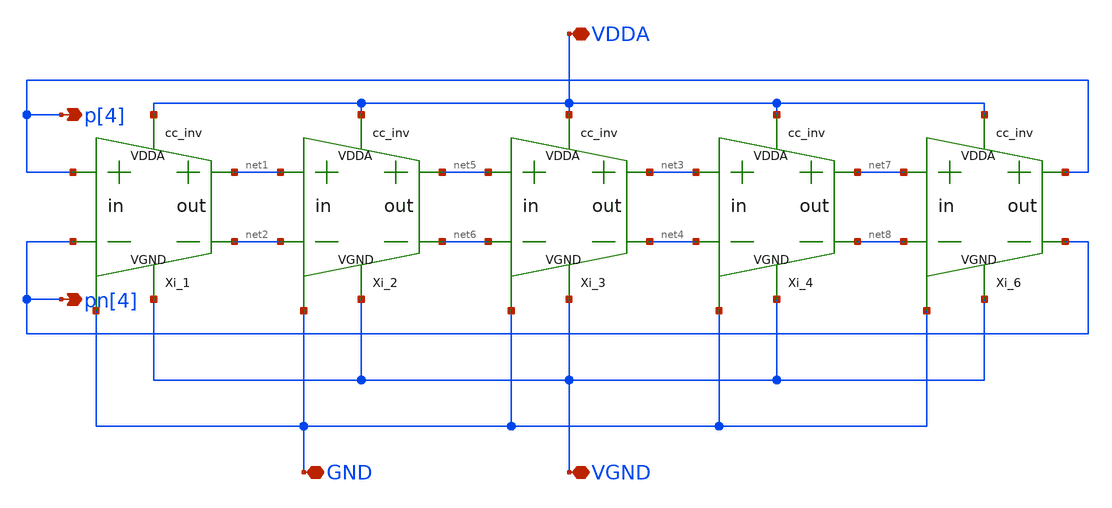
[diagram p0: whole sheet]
** sch_path: xschem/lib/x5s_cc_osc.sch
**.subckt x5s_cc_osc VDDA VGND p[4] pn[4] GND
*.iopin VDDA
*.iopin VGND
*.opin p[4]
*.opin pn[4]
*.iopin GND
Xi_1 p[4] pn[4] net1 net2 VGND VDDA GND cc_inv
Xi_2 net1 net2 net5 net6 VGND VDDA GND cc_inv
Xi_3 net5 net6 net3 net4 VGND VDDA GND cc_inv
Xi_4 net3 net4 net7 net8 VGND VDDA GND cc_inv
Xi_6 net7 net8 p[4] pn[4] VGND VDDA GND cc_inv
**.ends
.end
